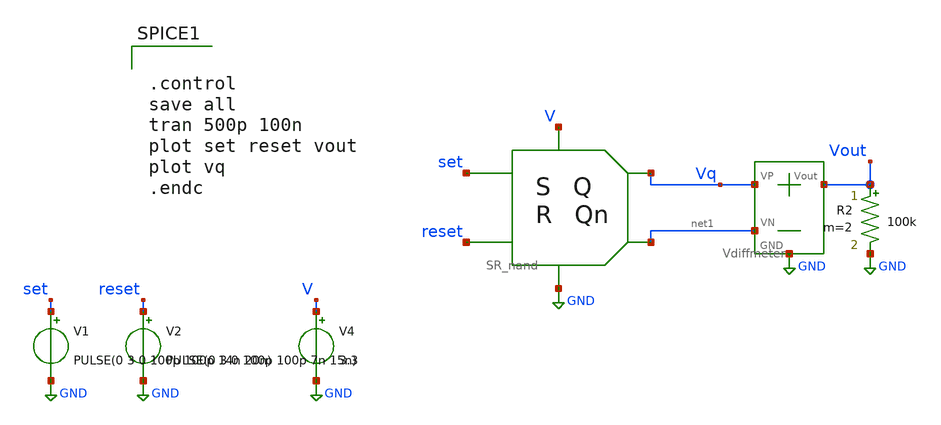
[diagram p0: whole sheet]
** sch_path: SAR_ADC/xschem/test/sr_latch_tb/latch_rs-1__tb.sch
**.subckt latch_rs-1__tb
V1 set GND PULSE(0 3 0 100p 100p 14n 20n)
V2 reset GND PULSE(0 3 0 100p 100p 7n 15n)
V4 V GND 3.3
R2 Vout GND 100k m=2
X1 set V GND reset Vq net1 SR_nand
X2 Vq net1 Vout GND Vdiffmeter
**** begin user architecture code


.control
save all
tran 500p 100n
plot set reset vout
plot vq
.endc


.include /foss/pdks/gf180mcuC/libs.tech/ngspice/design.ngspice
.lib /foss/pdks/gf180mcuC/libs.tech/ngspice/sm141064.ngspice typical

**** end user architecture code
**.ends

* expanding   symbol:  ../../../symbols/SR_nand.sym # of pins=6
** sym_path: SAR_ADC/xschem/designs/SR_nand.sym
** sch_path: SAR_ADC/xschem/designs/SR_nand.sch
.subckt SR_nand S V GND R Q Qn
*.iopin S
*.iopin R
*.iopin V
*.iopin GND
*.iopin Qn
*.iopin Q
XM1 V S Qn V sky130_fd_pr__pfet_03v3 L=0.28u W=1u nf=1 ad='int((nf+1)/2) * W/nf * 0.18u' as='int((nf+2)/2) * W/nf * 0.18u'
+ pd='2*int((nf+1)/2) * (W/nf + 0.18u)' ps='2*int((nf+2)/2) * (W/nf + 0.18u)' nrd='0.18u / W' nrs='0.18u / W'
+ sa=0 sb=0 sd=0 mult=1 m=1
XM2 Qn Q net1 GND sky130_fd_pr__nfet_03v3 L=0.28u W=1u nf=1 ad='int((nf+1)/2) * W/nf * 0.18u' as='int((nf+2)/2) * W/nf * 0.18u'
+ pd='2*int((nf+1)/2) * (W/nf + 0.18u)' ps='2*int((nf+2)/2) * (W/nf + 0.18u)' nrd='0.18u / W' nrs='0.18u / W'
+ sa=0 sb=0 sd=0 mult=1 m=1
XM3 V Qn Q V sky130_fd_pr__pfet_03v3 L=0.28u W=1u nf=1 ad='int((nf+1)/2) * W/nf * 0.18u' as='int((nf+2)/2) * W/nf * 0.18u'
+ pd='2*int((nf+1)/2) * (W/nf + 0.18u)' ps='2*int((nf+2)/2) * (W/nf + 0.18u)' nrd='0.18u / W' nrs='0.18u / W'
+ sa=0 sb=0 sd=0 mult=1 m=1
XM4 V R Q V sky130_fd_pr__pfet_03v3 L=0.28u W=1u nf=1 ad='int((nf+1)/2) * W/nf * 0.18u' as='int((nf+2)/2) * W/nf * 0.18u'
+ pd='2*int((nf+1)/2) * (W/nf + 0.18u)' ps='2*int((nf+2)/2) * (W/nf + 0.18u)' nrd='0.18u / W' nrs='0.18u / W'
+ sa=0 sb=0 sd=0 mult=1 m=1
XM5 V Q Qn V sky130_fd_pr__pfet_03v3 L=0.28u W=1u nf=1 ad='int((nf+1)/2) * W/nf * 0.18u' as='int((nf+2)/2) * W/nf * 0.18u'
+ pd='2*int((nf+1)/2) * (W/nf + 0.18u)' ps='2*int((nf+2)/2) * (W/nf + 0.18u)' nrd='0.18u / W' nrs='0.18u / W'
+ sa=0 sb=0 sd=0 mult=1 m=1
XM6 net1 S GND GND sky130_fd_pr__nfet_03v3 L=0.28u W=1u nf=1 ad='int((nf+1)/2) * W/nf * 0.18u' as='int((nf+2)/2) * W/nf * 0.18u'
+ pd='2*int((nf+1)/2) * (W/nf + 0.18u)' ps='2*int((nf+2)/2) * (W/nf + 0.18u)' nrd='0.18u / W' nrs='0.18u / W'
+ sa=0 sb=0 sd=0 mult=1 m=1
XM7 Q Qn net2 GND sky130_fd_pr__nfet_03v3 L=0.28u W=1u nf=1 ad='int((nf+1)/2) * W/nf * 0.18u' as='int((nf+2)/2) * W/nf * 0.18u'
+ pd='2*int((nf+1)/2) * (W/nf + 0.18u)' ps='2*int((nf+2)/2) * (W/nf + 0.18u)' nrd='0.18u / W' nrs='0.18u / W'
+ sa=0 sb=0 sd=0 mult=1 m=1
XM8 net2 R GND GND sky130_fd_pr__nfet_03v3 L=0.28u W=1u nf=1 ad='int((nf+1)/2) * W/nf * 0.18u' as='int((nf+2)/2) * W/nf * 0.18u'
+ pd='2*int((nf+1)/2) * (W/nf + 0.18u)' ps='2*int((nf+2)/2) * (W/nf + 0.18u)' nrd='0.18u / W' nrs='0.18u / W'
+ sa=0 sb=0 sd=0 mult=1 m=1
.ends


* expanding   symbol:  ../../../symbols/Vdiffmeter.sym # of pins=4
** sym_path: SAR_ADC/xschem/spice/symbols/Vdiffmeter.sym
** sch_path: SAR_ADC/xschem/spice/symbols/Vdiffmeter.sch
.subckt Vdiffmeter VP VN Vout GND
*.iopin Vout
*.iopin GND
*.iopin VP
*.iopin VN
R4 Vout GND 1k m=1
E4 Vout GND VP VN 1
.ends

.GLOBAL GND
.end
